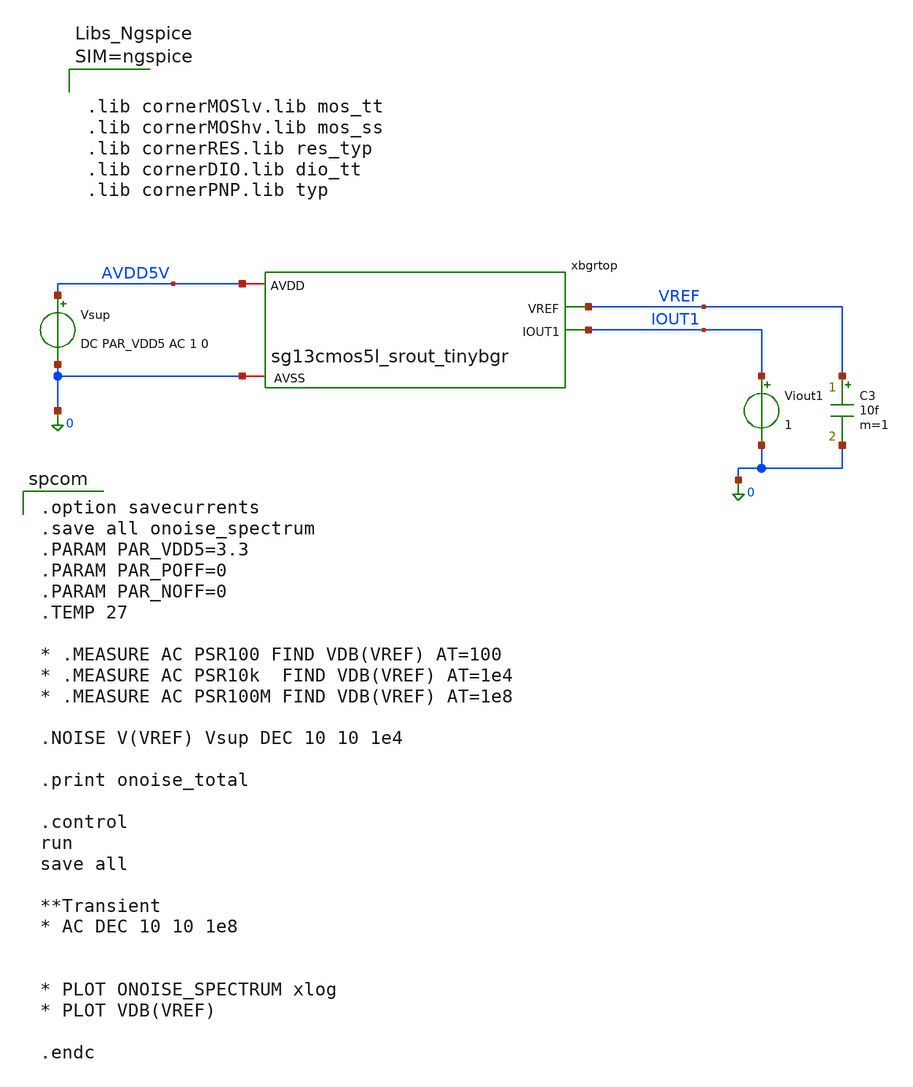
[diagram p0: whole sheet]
** sch_path: xschem/TB_tinybgr_AC.sch
**.subckt TB_tinybgr_AC
Vsup AVDD5V 0 DC PAR_VDD5 AC 1 0
C3 VREF 0 10f m=1
Viout1 IOUT1 0 1
xbgrtop AVDD5V VREF IOUT1 0 sg13cmos5l_srout_tinybgr
**** begin user architecture code

.option savecurrents
.save all onoise_spectrum
.PARAM PAR_VDD5=3.3
.PARAM PAR_POFF=0
.PARAM PAR_NOFF=0
.TEMP 27

* .MEASURE AC PSR100 FIND VDB(VREF) AT=100
* .MEASURE AC PSR10k  FIND VDB(VREF) AT=1e4
* .MEASURE AC PSR100M FIND VDB(VREF) AT=1e8

.NOISE V(VREF) Vsup DEC 10 10 1e4

.print onoise_total

.control
run
save all

**Transient
* AC DEC 10 10 1e8


* PLOT ONOISE_SPECTRUM xlog
* PLOT VDB(VREF)

.endc




.lib cornerMOSlv.lib mos_tt
.lib cornerMOShv.lib mos_ss
.lib cornerRES.lib res_typ
.lib cornerDIO.lib dio_tt
.lib cornerPNP.lib typ



**** end user architecture code
**.ends

* expanding   symbol:  sg13cmos5l_srout_tinybgr.sym # of pins=4
** sym_path: xschem/sg13cmos5l_srout_tinybgr.sym
** sch_path: xschem/sg13cmos5l_srout_tinybgr.sch
.subckt sg13cmos5l_srout_tinybgr AVDD VREF IOUT1 AVSS
*.iopin AVDD
*.iopin AVSS
*.opin VREF
*.opin IOUT1
XQ1 AVSS AVSS Vbe1 pnpMPA a=2p p=6u m=8
XQ2 AVSS AVSS Vbe2 pnpMPA a=2p p=6u m=1
XMN2 Vgn Vgn Vbe2 AVSS sg13_hv_nmos w=2.6u l=1u ng=1 m=6 mm_ok=1
XMN1 Vgp Vgn Vbe2mr AVSS sg13_hv_nmos w=2.6u l=1u ng=1 m=12 mm_ok=1
XMP2 Vgn Vgp AVDD AVDD sg13_hv_pmos w=1u l=4u ng=1 m=3 mm_ok=1
XMP1 Vgp Vgp AVDD AVDD sg13_hv_pmos w=1u l=4u ng=1 m=6 mm_ok=1
XMP3 IOUT1 Vgp AVDD AVDD sg13_hv_pmos w=1u l=4u ng=1 m=11 mm_ok=1
XMP5 VREF Vgp AVDD AVDD sg13_hv_pmos w=1u l=4u ng=1 m=3 mm_ok=1
XMNSU1 AVDD vgsu1 Vgn AVSS sg13_hv_nmos w=1u l=2u ng=1 m=1 mm_ok=1
XMPSU1 net1 VREF AVDD AVDD sg13_hv_pmos w=0.35u l=6u ng=1 m=1 mm_ok=1
XMNSU2 vgsu1 VREF AVSS AVSS sg13_hv_nmos w=1u l=1u ng=1 m=1 mm_ok=1
XMPSU2 net2 VREF net1 AVDD sg13_hv_pmos w=0.35u l=6u ng=1 m=1 mm_ok=1
XMPSU3 net3 VREF net2 AVDD sg13_hv_pmos w=0.35u l=6u ng=1 m=1 mm_ok=1
XMPSU4 vgsu1 VREF net3 AVDD sg13_hv_pmos w=0.35u l=6u ng=1 m=1 mm_ok=1
xbgrres VREF Vbe2mr AVSS Vbe2 Vbe1 sg13cmos5l_srout_tinybgr_res
XQ3 AVSS AVSS AVSS pnpMPA a=2p p=6u m=2
XMN3 AVSS AVSS AVSS AVSS sg13_hv_nmos w=2.6u l=1u ng=1 m=2 mm_ok=1
XMN4 Vgn AVSS AVSS AVSS sg13_hv_nmos w=2.6u l=1u ng=1 m=2 mm_ok=1
XMN5 Vgp AVSS AVSS AVSS sg13_hv_nmos w=2.6u l=1u ng=1 m=4 mm_ok=1
XMP4 AVDD Vgp AVDD AVDD sg13_hv_pmos w=1u l=4u ng=1 m=4 mm_ok=1
XMP6 Vgn AVDD AVDD AVDD sg13_hv_pmos w=1u l=4u ng=1 m=1 mm_ok=1
XMP7 IOUT1 AVDD AVDD AVDD sg13_hv_pmos w=1u l=4u ng=1 m=1 mm_ok=1
XMP8 VREF AVDD AVDD AVDD sg13_hv_pmos w=1u l=4u ng=1 m=1 mm_ok=1
XMP9 AVDD AVDD AVDD AVDD sg13_hv_pmos w=1u l=4u ng=1 m=9 mm_ok=1
.ends


* expanding   symbol:  sg13cmos5l_srout_tinybgr_res.sym # of pins=5
** sym_path: xschem/sg13cmos5l_srout_tinybgr_res.sym
** sch_path: xschem/sg13cmos5l_srout_tinybgr_res.sch
.subckt sg13cmos5l_srout_tinybgr_res Vref Vbe2mr AVSS Vbe2 Vbe1
*.iopin Vbe1
*.iopin Vbe2
*.iopin AVSS
*.iopin Vbe2mr
*.iopin Vref
XR3 Vbe2mr net21 AVSS rhigh w=1.1u l=4u m=1 b=0 mm_ok=1
XR1 net21 Vbe1 AVSS rhigh w=1.1u l=4u m=1 b=0 mm_ok=1
XR2 net2 net1 AVSS rhigh w=1.1u l=4u m=1 b=0 mm_ok=1
XR4 net1 Vbe2 AVSS rhigh w=1.1u l=4u m=1 b=0 mm_ok=1
XR5 net3 net2 AVSS rhigh w=1.1u l=4u m=1 b=0 mm_ok=1
XR6 net4 net3 AVSS rhigh w=1.1u l=4u m=1 b=0 mm_ok=1
XR7 net22 net4 AVSS rhigh w=1.1u l=4u m=1 b=0 mm_ok=1
XR8 net6 net5 AVSS rhigh w=1.1u l=4u m=1 b=0 mm_ok=1
XR9 net5 net23 AVSS rhigh w=1.1u l=4u m=1 b=0 mm_ok=1
XR10 net7 net6 AVSS rhigh w=1.1u l=4u m=1 b=0 mm_ok=1
XR11 net8 net7 AVSS rhigh w=1.1u l=4u m=1 b=0 mm_ok=1
XR12 net22 net8 AVSS rhigh w=1.1u l=4u m=1 b=0 mm_ok=1
XR13 net10 net9 AVSS rhigh w=1.1u l=4u m=1 b=0 mm_ok=1
XR14 net9 net23 AVSS rhigh w=1.1u l=4u m=1 b=0 mm_ok=1
XR15 net11 net10 AVSS rhigh w=1.1u l=4u m=1 b=0 mm_ok=1
XR16 net12 net11 AVSS rhigh w=1.1u l=4u m=1 b=0 mm_ok=1
XR17 net24 net12 AVSS rhigh w=1.1u l=4u m=1 b=0 mm_ok=1
XR18 net14 net13 AVSS rhigh w=1.1u l=4u m=1 b=0 mm_ok=1
XR19 net13 net25 AVSS rhigh w=1.1u l=4u m=1 b=0 mm_ok=1
XR20 net15 net14 AVSS rhigh w=1.1u l=4u m=1 b=0 mm_ok=1
XR21 net16 net15 AVSS rhigh w=1.1u l=4u m=1 b=0 mm_ok=1
XR22 net24 net16 AVSS rhigh w=1.1u l=4u m=1 b=0 mm_ok=1
XR23 net18 net17 AVSS rhigh w=1.1u l=4u m=1 b=0 mm_ok=1
XR24 net17 net26 AVSS rhigh w=1.1u l=4u m=1 b=0 mm_ok=1
XR25 net19 net18 AVSS rhigh w=1.1u l=4u m=1 b=0 mm_ok=1
XR26 net20 net19 AVSS rhigh w=1.1u l=4u m=1 b=0 mm_ok=1
XR27 Vref net20 AVSS rhigh w=1.1u l=4u m=1 b=0 mm_ok=1
XR28 net25 net27 AVSS rhigh w=1.1u l=4u m=1 b=0 mm_ok=1
XR29 net26 net27 AVSS rhigh w=1.1u l=4u m=1 b=0 mm_ok=1
XR30 AVSS AVSS AVSS rhigh w=1.1u l=4u m=9 b=0 mm_ok=1
.ends

.end
